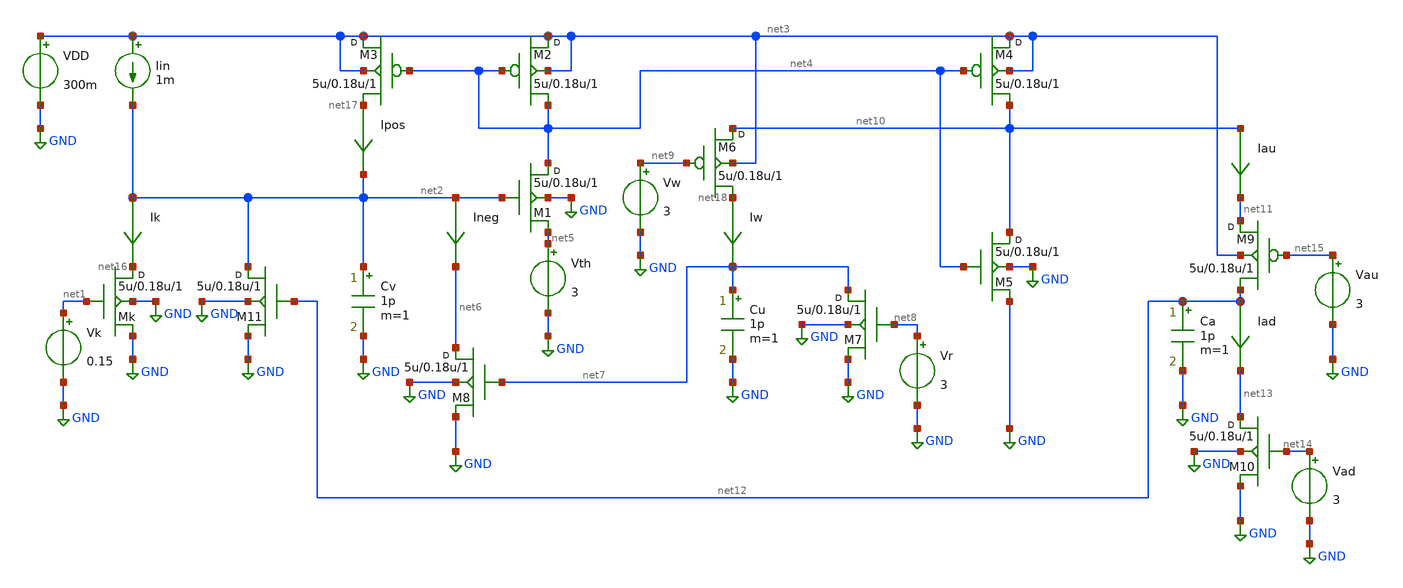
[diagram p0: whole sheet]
** sch_path: xschem/untitled.sch
**.subckt untitled
Iin net3 net2 1m
Mk net16 net1 GND GND nmos w=5u l=0.18u m=1
Ik net2 net16 0
.save i(ik)
Vk net1 GND 0.15
VDD net3 GND 300m
M11 net2 net12 GND GND nmos w=5u l=0.18u m=1
Cv net2 GND 1p m=1
Ipos net17 net2 0
.save i(ipos)
M2 net3 net4 net4 net3 pmos w=5u l=0.18u m=1
M3 net3 net4 net17 net3 pmos w=5u l=0.18u m=1
M1 net4 net2 net5 GND nmos w=5u l=0.18u m=1
Ineg net2 net6 0
.save i(ineg)
Vth net5 GND 3
M8 net6 net7 GND GND nmos w=5u l=0.18u m=1
Cu net7 GND 1p m=1
M6 net10 net9 net18 net3 pmos w=5u l=0.18u m=1
M7 net7 net8 GND GND nmos w=5u l=0.18u m=1
Vr net8 GND 3
Iw net18 net7 0
.save i(iw)
Vw net9 GND 3
M5 net10 net4 GND GND nmos w=5u l=0.18u m=1
M4 net3 net4 net10 net3 pmos w=5u l=0.18u m=1
Iad net12 net13 0
.save i(iad)
Iau net10 net11 0
.save i(iau)
Ca net12 GND 1p m=1
M9 net11 net15 net12 net3 pmos w=5u l=0.18u m=1
M10 net13 net14 GND GND nmos w=5u l=0.18u m=1
Vad net14 GND 3
Vau net15 GND 3
**** begin user architecture code





**** end user architecture code
**.ends
.GLOBAL GND
.end
